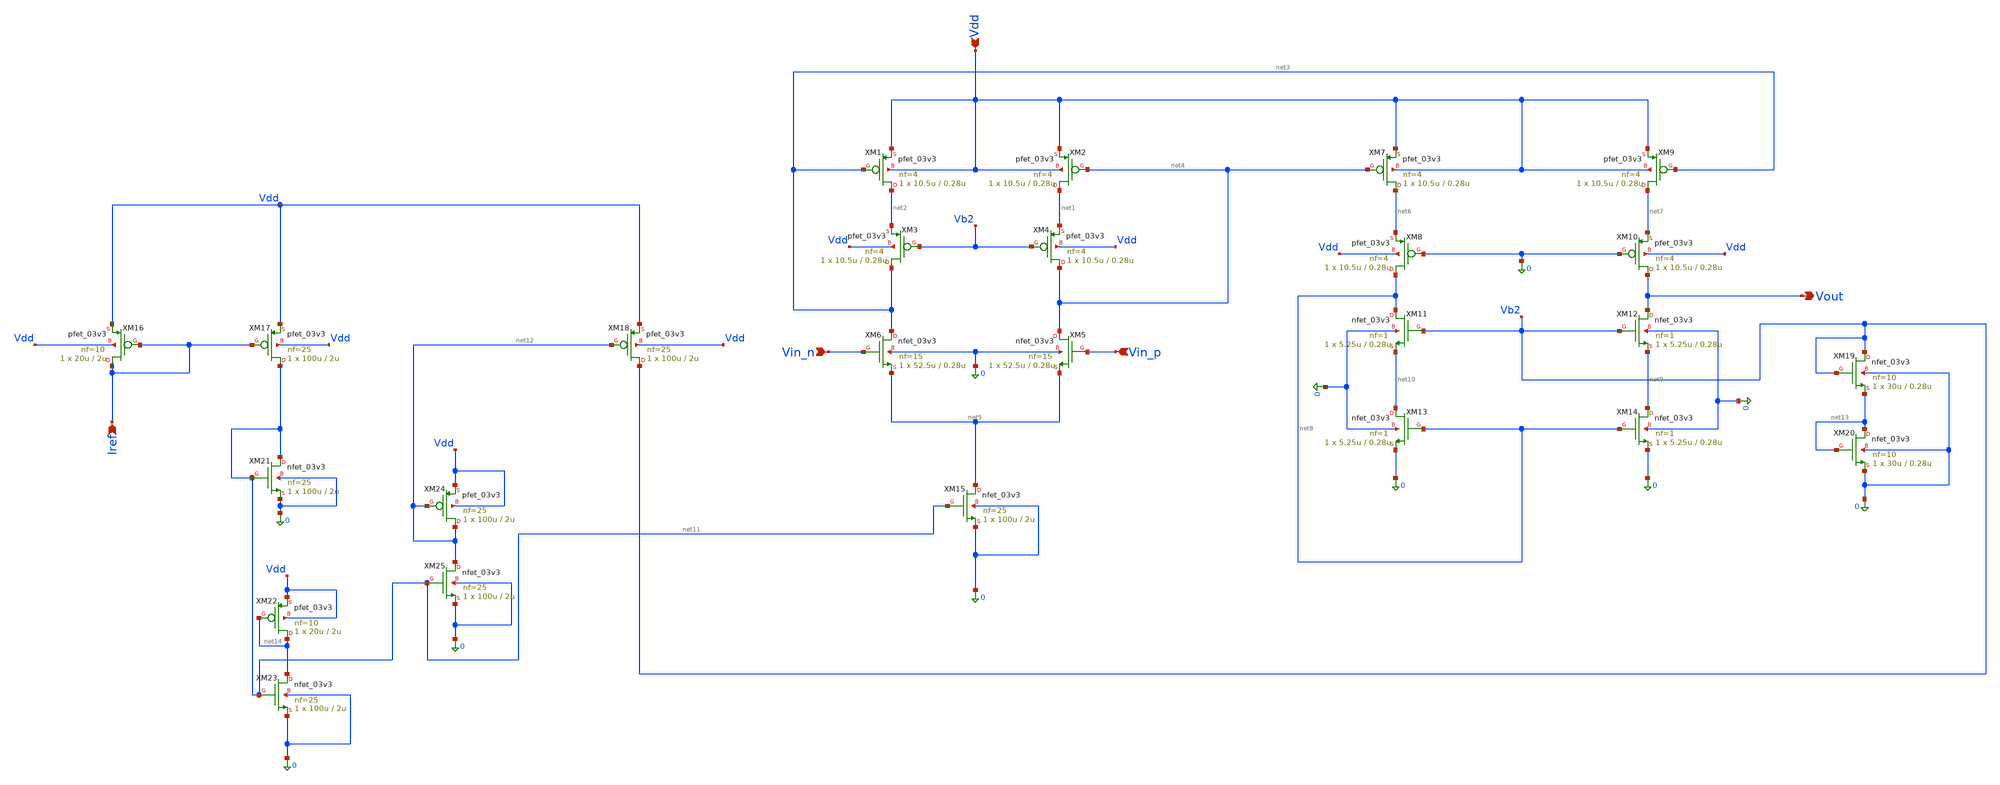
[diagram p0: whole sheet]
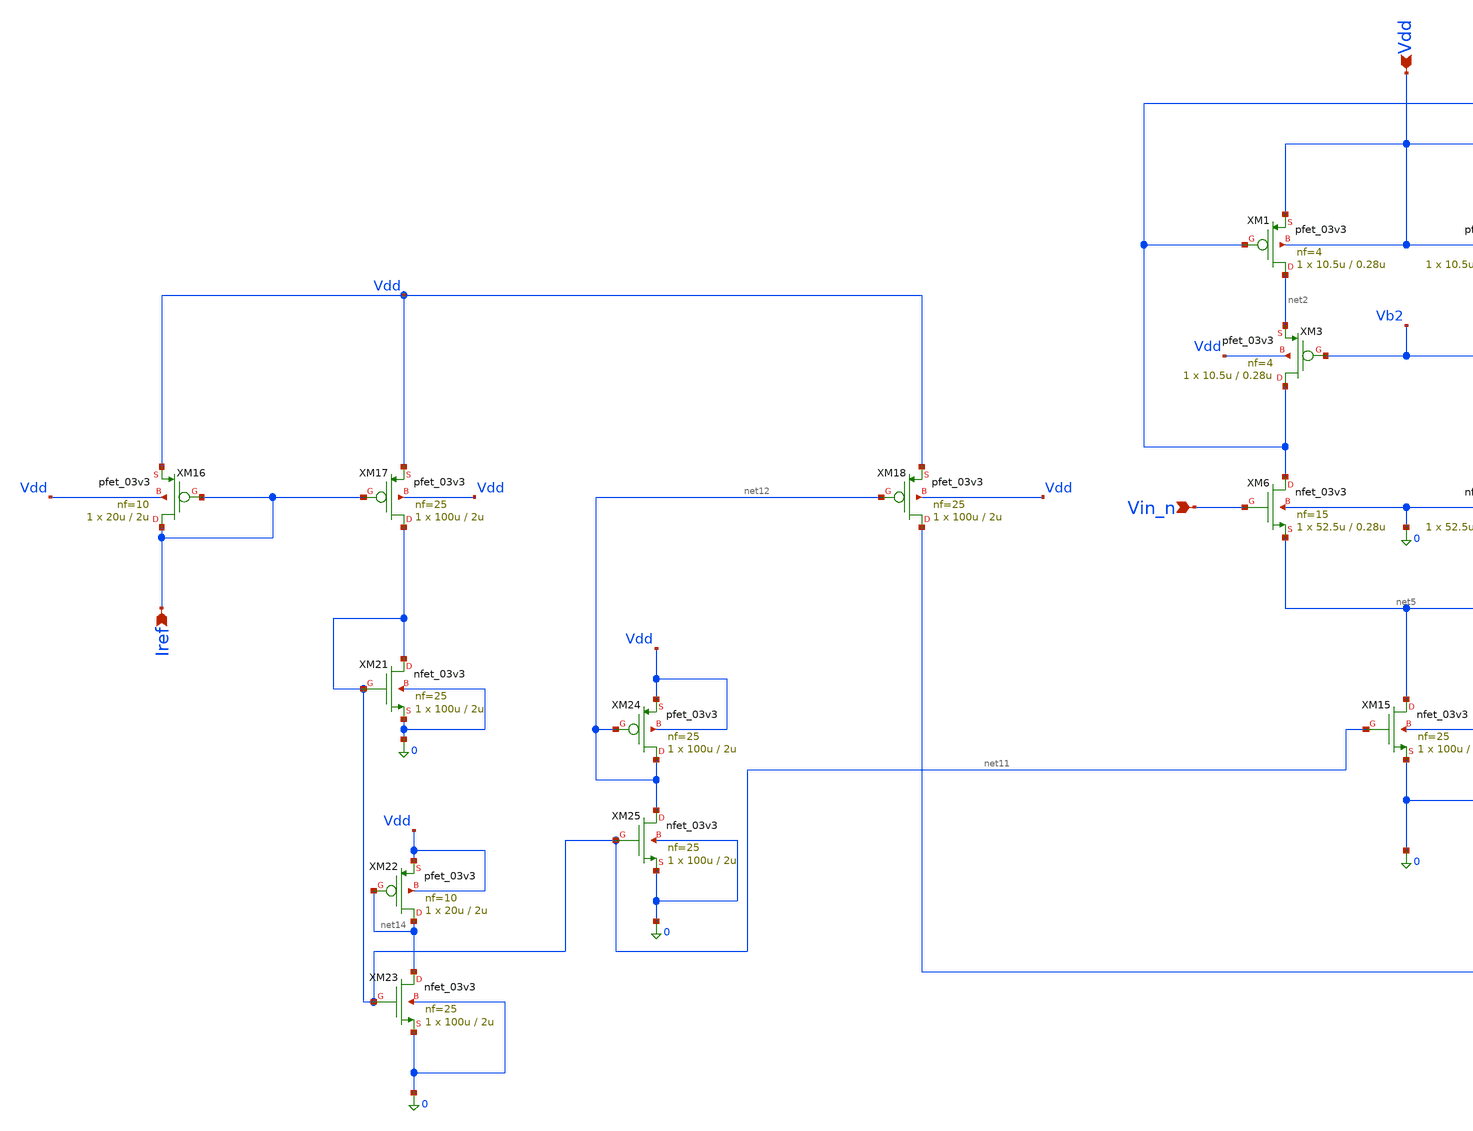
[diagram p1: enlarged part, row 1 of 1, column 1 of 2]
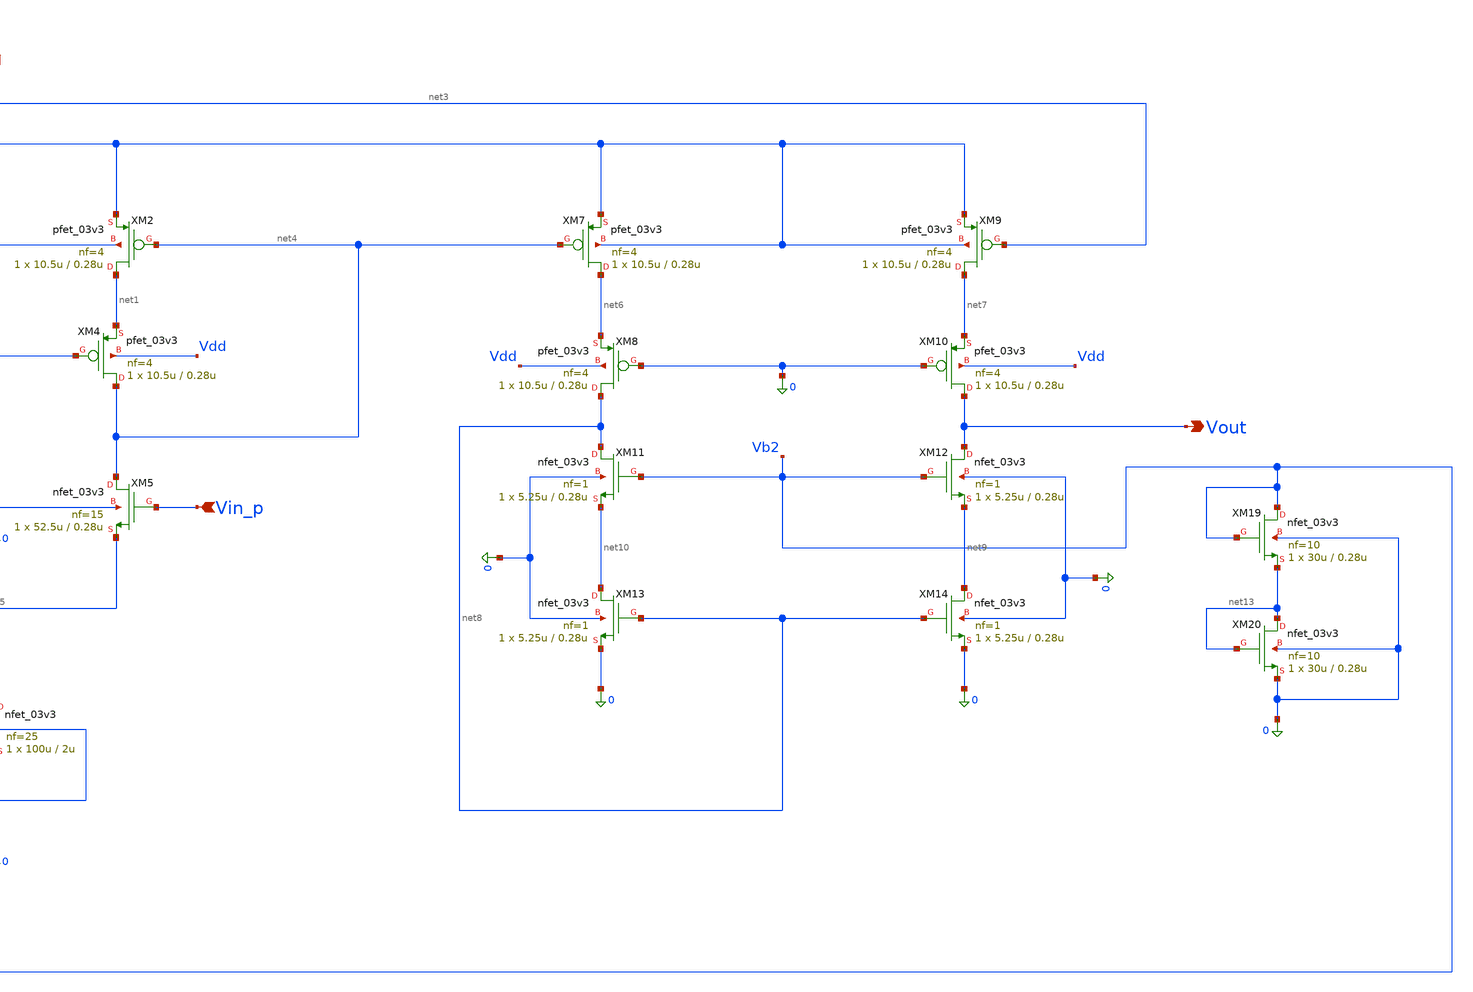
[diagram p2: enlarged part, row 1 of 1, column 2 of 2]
** sch_path: blocks/adc/lvds/op_amp.sch
**.subckt op_amp Vdd Vin_p Vin_n Vout Iref
*.ipin Vdd
*.ipin Vin_p
*.ipin Vin_n
*.opin Vout
*.ipin Iref
XM1 net2 net3 Vdd Vdd pfet_03v3 L=0.28u W=10.5u nf=4 ad='int((nf+1)/2) * W/nf * 0.18u' as='int((nf+2)/2) * W/nf * 0.18u'
+ pd='2*int((nf+1)/2) * (W/nf + 0.18u)' ps='2*int((nf+2)/2) * (W/nf + 0.18u)' nrd='0.18u / W' nrs='0.18u / W'
+ sa=0 sb=0 sd=0 m=1
XM2 net1 net4 Vdd Vdd pfet_03v3 L=0.28u W=10.5u nf=4 ad='int((nf+1)/2) * W/nf * 0.18u' as='int((nf+2)/2) * W/nf * 0.18u'
+ pd='2*int((nf+1)/2) * (W/nf + 0.18u)' ps='2*int((nf+2)/2) * (W/nf + 0.18u)' nrd='0.18u / W' nrs='0.18u / W'
+ sa=0 sb=0 sd=0 m=1
XM3 net3 Vb2 net2 Vdd pfet_03v3 L=0.28u W=10.5u nf=4 ad='int((nf+1)/2) * W/nf * 0.18u' as='int((nf+2)/2) * W/nf * 0.18u'
+ pd='2*int((nf+1)/2) * (W/nf + 0.18u)' ps='2*int((nf+2)/2) * (W/nf + 0.18u)' nrd='0.18u / W' nrs='0.18u / W'
+ sa=0 sb=0 sd=0 m=1
XM4 net4 Vb2 net1 Vdd pfet_03v3 L=0.28u W=10.5u nf=4 ad='int((nf+1)/2) * W/nf * 0.18u' as='int((nf+2)/2) * W/nf * 0.18u'
+ pd='2*int((nf+1)/2) * (W/nf + 0.18u)' ps='2*int((nf+2)/2) * (W/nf + 0.18u)' nrd='0.18u / W' nrs='0.18u / W'
+ sa=0 sb=0 sd=0 m=1
XM5 net4 Vin_p net5 0 nfet_03v3 L=0.28u W=52.5u nf=15 ad='int((nf+1)/2) * W/nf * 0.18u' as='int((nf+2)/2) * W/nf * 0.18u'
+ pd='2*int((nf+1)/2) * (W/nf + 0.18u)' ps='2*int((nf+2)/2) * (W/nf + 0.18u)' nrd='0.18u / W' nrs='0.18u / W'
+ sa=0 sb=0 sd=0 m=1
XM6 net3 Vin_n net5 0 nfet_03v3 L=0.28u W=52.5u nf=15 ad='int((nf+1)/2) * W/nf * 0.18u' as='int((nf+2)/2) * W/nf * 0.18u'
+ pd='2*int((nf+1)/2) * (W/nf + 0.18u)' ps='2*int((nf+2)/2) * (W/nf + 0.18u)' nrd='0.18u / W' nrs='0.18u / W'
+ sa=0 sb=0 sd=0 m=1
XM7 net6 net4 Vdd Vdd pfet_03v3 L=0.28u W=10.5u nf=4 ad='int((nf+1)/2) * W/nf * 0.18u' as='int((nf+2)/2) * W/nf * 0.18u'
+ pd='2*int((nf+1)/2) * (W/nf + 0.18u)' ps='2*int((nf+2)/2) * (W/nf + 0.18u)' nrd='0.18u / W' nrs='0.18u / W'
+ sa=0 sb=0 sd=0 m=1
XM9 net7 net3 Vdd Vdd pfet_03v3 L=0.28u W=10.5u nf=4 ad='int((nf+1)/2) * W/nf * 0.18u' as='int((nf+2)/2) * W/nf * 0.18u'
+ pd='2*int((nf+1)/2) * (W/nf + 0.18u)' ps='2*int((nf+2)/2) * (W/nf + 0.18u)' nrd='0.18u / W' nrs='0.18u / W'
+ sa=0 sb=0 sd=0 m=1
XM11 net8 Vb2 net10 0 nfet_03v3 L=0.28u W=5.25u nf=1 ad='int((nf+1)/2) * W/nf * 0.18u' as='int((nf+2)/2) * W/nf * 0.18u'
+ pd='2*int((nf+1)/2) * (W/nf + 0.18u)' ps='2*int((nf+2)/2) * (W/nf + 0.18u)' nrd='0.18u / W' nrs='0.18u / W'
+ sa=0 sb=0 sd=0 m=1
XM12 Vout Vb2 net9 0 nfet_03v3 L=0.28u W=5.25u nf=1 ad='int((nf+1)/2) * W/nf * 0.18u' as='int((nf+2)/2) * W/nf * 0.18u'
+ pd='2*int((nf+1)/2) * (W/nf + 0.18u)' ps='2*int((nf+2)/2) * (W/nf + 0.18u)' nrd='0.18u / W' nrs='0.18u / W'
+ sa=0 sb=0 sd=0 m=1
XM13 net10 net8 0 0 nfet_03v3 L=0.28u W=5.25u nf=1 ad='int((nf+1)/2) * W/nf * 0.18u' as='int((nf+2)/2) * W/nf * 0.18u'
+ pd='2*int((nf+1)/2) * (W/nf + 0.18u)' ps='2*int((nf+2)/2) * (W/nf + 0.18u)' nrd='0.18u / W' nrs='0.18u / W'
+ sa=0 sb=0 sd=0 m=1
XM14 net9 net8 0 0 nfet_03v3 L=0.28u W=5.25u nf=1 ad='int((nf+1)/2) * W/nf * 0.18u' as='int((nf+2)/2) * W/nf * 0.18u'
+ pd='2*int((nf+1)/2) * (W/nf + 0.18u)' ps='2*int((nf+2)/2) * (W/nf + 0.18u)' nrd='0.18u / W' nrs='0.18u / W'
+ sa=0 sb=0 sd=0 m=1
XM8 net8 0 net6 Vdd pfet_03v3 L=0.28u W=10.5u nf=4 ad='int((nf+1)/2) * W/nf * 0.18u' as='int((nf+2)/2) * W/nf * 0.18u'
+ pd='2*int((nf+1)/2) * (W/nf + 0.18u)' ps='2*int((nf+2)/2) * (W/nf + 0.18u)' nrd='0.18u / W' nrs='0.18u / W'
+ sa=0 sb=0 sd=0 m=1
XM10 Vout 0 net7 Vdd pfet_03v3 L=0.28u W=10.5u nf=4 ad='int((nf+1)/2) * W/nf * 0.18u' as='int((nf+2)/2) * W/nf * 0.18u'
+ pd='2*int((nf+1)/2) * (W/nf + 0.18u)' ps='2*int((nf+2)/2) * (W/nf + 0.18u)' nrd='0.18u / W' nrs='0.18u / W'
+ sa=0 sb=0 sd=0 m=1
XM15 net5 net11 0 0 nfet_03v3 L=2u W=100u nf=25 ad='int((nf+1)/2) * W/nf * 0.18u' as='int((nf+2)/2) * W/nf * 0.18u'
+ pd='2*int((nf+1)/2) * (W/nf + 0.18u)' ps='2*int((nf+2)/2) * (W/nf + 0.18u)' nrd='0.18u / W' nrs='0.18u / W'
+ sa=0 sb=0 sd=0 m=1
XM16 Iref Iref Vdd Vdd pfet_03v3 L=2u W=20u nf=10 ad='int((nf+1)/2) * W/nf * 0.18u' as='int((nf+2)/2) * W/nf * 0.18u'
+ pd='2*int((nf+1)/2) * (W/nf + 0.18u)' ps='2*int((nf+2)/2) * (W/nf + 0.18u)' nrd='0.18u / W' nrs='0.18u / W'
+ sa=0 sb=0 sd=0 m=1
XM17 net11 Iref Vdd Vdd pfet_03v3 L=2u W=100u nf=25 ad='int((nf+1)/2) * W/nf * 0.18u' as='int((nf+2)/2) * W/nf * 0.18u'
+ pd='2*int((nf+1)/2) * (W/nf + 0.18u)' ps='2*int((nf+2)/2) * (W/nf + 0.18u)' nrd='0.18u / W' nrs='0.18u / W'
+ sa=0 sb=0 sd=0 m=1
XM19 Vb2 Vb2 net13 0 nfet_03v3 L=0.28u W=30u nf=10 ad='int((nf+1)/2) * W/nf * 0.18u' as='int((nf+2)/2) * W/nf * 0.18u'
+ pd='2*int((nf+1)/2) * (W/nf + 0.18u)' ps='2*int((nf+2)/2) * (W/nf + 0.18u)' nrd='0.18u / W' nrs='0.18u / W'
+ sa=0 sb=0 sd=0 m=1
XM20 net13 net13 0 0 nfet_03v3 L=0.28u W=30u nf=10 ad='int((nf+1)/2) * W/nf * 0.18u' as='int((nf+2)/2) * W/nf * 0.18u'
+ pd='2*int((nf+1)/2) * (W/nf + 0.18u)' ps='2*int((nf+2)/2) * (W/nf + 0.18u)' nrd='0.18u / W' nrs='0.18u / W'
+ sa=0 sb=0 sd=0 m=1
XM21 net11 net11 0 0 nfet_03v3 L=2u W=100u nf=25 ad='int((nf+1)/2) * W/nf * 0.18u' as='int((nf+2)/2) * W/nf * 0.18u'
+ pd='2*int((nf+1)/2) * (W/nf + 0.18u)' ps='2*int((nf+2)/2) * (W/nf + 0.18u)' nrd='0.18u / W' nrs='0.18u / W'
+ sa=0 sb=0 sd=0 m=1
XM18 Vb2 net12 Vdd Vdd pfet_03v3 L=2u W=100u nf=25 ad='int((nf+1)/2) * W/nf * 0.18u' as='int((nf+2)/2) * W/nf * 0.18u'
+ pd='2*int((nf+1)/2) * (W/nf + 0.18u)' ps='2*int((nf+2)/2) * (W/nf + 0.18u)' nrd='0.18u / W' nrs='0.18u / W'
+ sa=0 sb=0 sd=0 m=1
XM22 net14 net14 Vdd Vdd pfet_03v3 L=2u W=20u nf=10 ad='int((nf+1)/2) * W/nf * 0.18u' as='int((nf+2)/2) * W/nf * 0.18u'
+ pd='2*int((nf+1)/2) * (W/nf + 0.18u)' ps='2*int((nf+2)/2) * (W/nf + 0.18u)' nrd='0.18u / W' nrs='0.18u / W'
+ sa=0 sb=0 sd=0 m=1
XM23 net14 net11 0 0 nfet_03v3 L=2u W=100u nf=25 ad='int((nf+1)/2) * W/nf * 0.18u' as='int((nf+2)/2) * W/nf * 0.18u'
+ pd='2*int((nf+1)/2) * (W/nf + 0.18u)' ps='2*int((nf+2)/2) * (W/nf + 0.18u)' nrd='0.18u / W' nrs='0.18u / W'
+ sa=0 sb=0 sd=0 m=1
XM24 net12 net12 Vdd Vdd pfet_03v3 L=2u W=100u nf=25 ad='int((nf+1)/2) * W/nf * 0.18u' as='int((nf+2)/2) * W/nf * 0.18u'
+ pd='2*int((nf+1)/2) * (W/nf + 0.18u)' ps='2*int((nf+2)/2) * (W/nf + 0.18u)' nrd='0.18u / W' nrs='0.18u / W'
+ sa=0 sb=0 sd=0 m=1
XM25 net12 net11 0 0 nfet_03v3 L=2u W=100u nf=25 ad='int((nf+1)/2) * W/nf * 0.18u' as='int((nf+2)/2) * W/nf * 0.18u'
+ pd='2*int((nf+1)/2) * (W/nf + 0.18u)' ps='2*int((nf+2)/2) * (W/nf + 0.18u)' nrd='0.18u / W' nrs='0.18u / W'
+ sa=0 sb=0 sd=0 m=1
**.ends
.end
